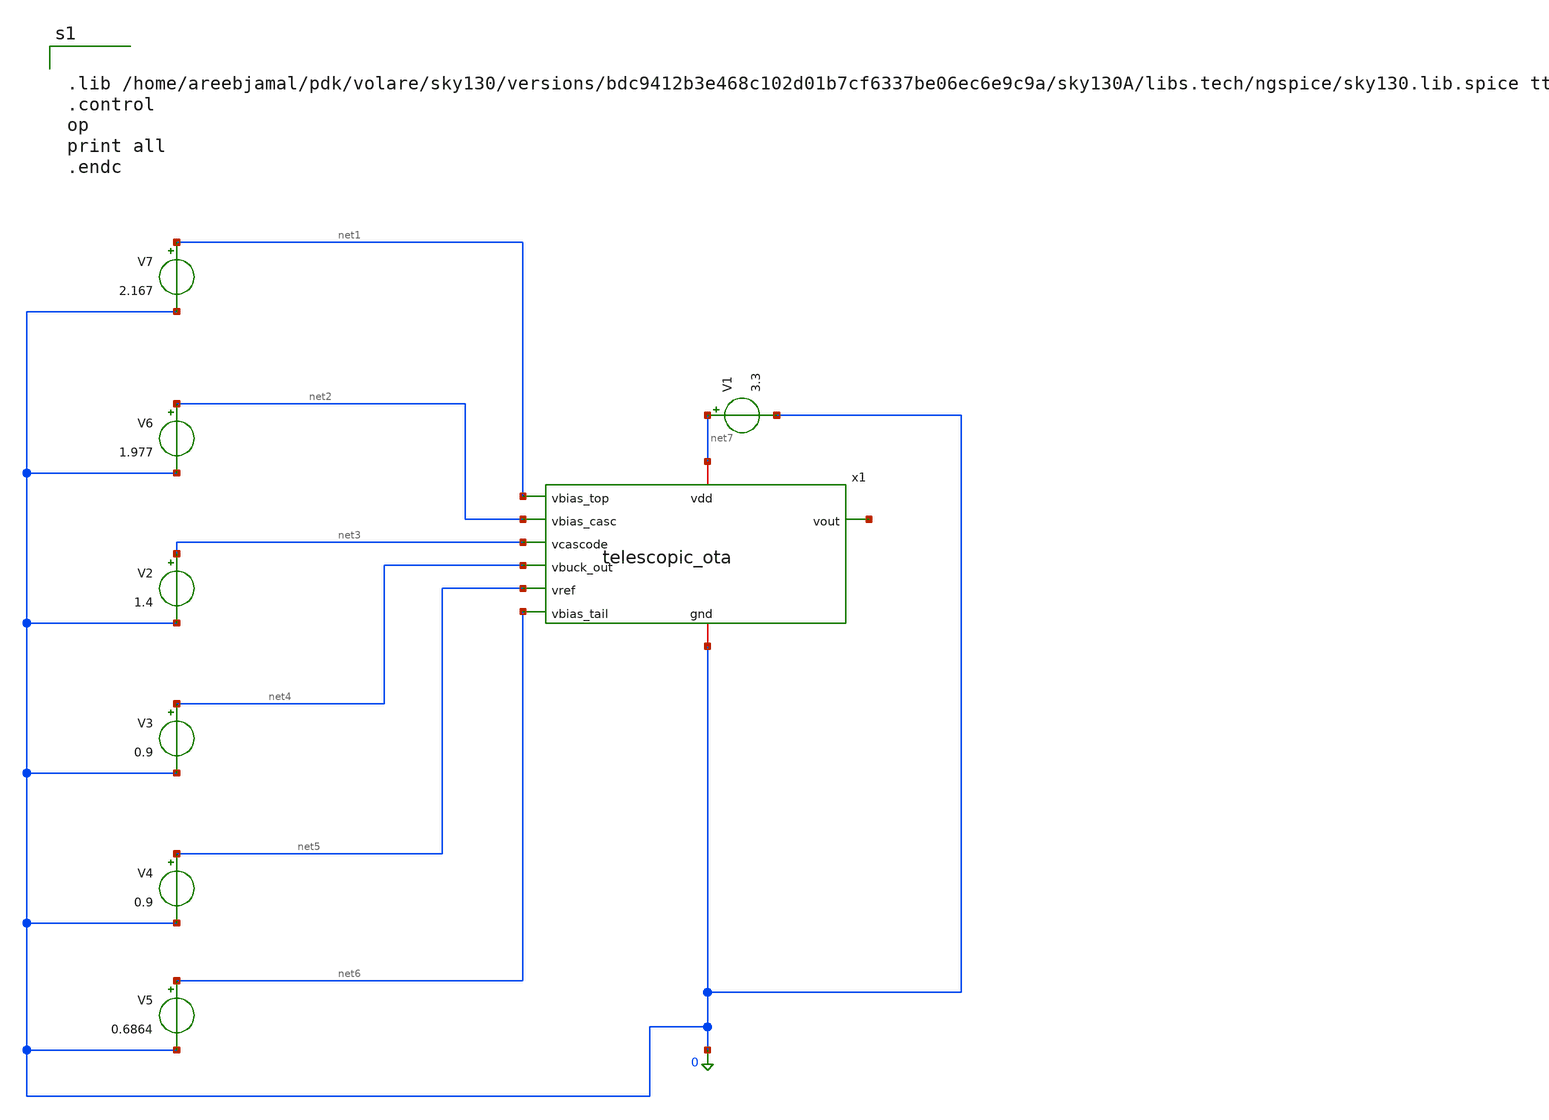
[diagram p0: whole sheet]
** sch_path: test_ota.sch
**.subckt test_ota
x1 net7 net1 net2 net8 net3 net4 net5 net6 0 telescopic_ota
V2 net3 0 1.4
V3 net4 0 0.9
V4 net5 0 0.9
V5 net6 0 0.6864
V6 net2 0 1.977
V7 net1 0 2.167
V1 net7 0 3.3
**** begin user architecture code


.lib /home/areebjamal/pdk/volare/sky130/versions/bdc9412b3e468c102d01b7cf6337be06ec6e9c9a/sky130A/libs.tech/ngspice/sky130.lib.spice tt
.control
op
print all
.endc


**** end user architecture code
**.ends

* expanding   symbol:  telescopic_ota.sym # of pins=9
** sym_path: telescopic_ota.sym
** sch_path: telescopic_ota.sch
.subckt telescopic_ota vdd vbias_top vbias_casc vout vcascode vbuck_out vref vbias_tail gnd
*.ipin vbias_top
*.ipin vbias_casc
*.ipin vcascode
*.ipin vbuck_out
*.ipin vref
*.ipin vbias_tail
*.opin vout
*.iopin vdd
*.iopin gnd
XM3 net3 vcascode vy gnd sky130_fd_pr__nfet_01v8 L=1 W=5.6 nf=1 ad='int((1 + 1)/2) * 5.6 / 1 * 0.29'
+ as='int((1 + 2)/2) * 5.6 / 1 * 0.29' pd='2*int((1 + 1)/2) * (5.6 / 1 + 0.29)' ps='2*int((1 + 2)/2) * (5.6 / 1 + 0.29)'
+ nrd='0.29 / 5.6 ' nrs='0.29 / 5.6 ' sa=0 sb=0 sd=0 mult=1 m=1
XM8 net2 vbias_top vdd vdd sky130_fd_pr__pfet_01v8 L=1 W=16.8 nf=1 ad='int((1 + 1)/2) * 16.8 / 1 * 0.29'
+ as='int((1 + 2)/2) * 16.8 / 1 * 0.29' pd='2*int((1 + 1)/2) * (16.8 / 1 + 0.29)' ps='2*int((1 + 2)/2) * (16.8 / 1 + 0.29)'
+ nrd='0.29 / 16.8 ' nrs='0.29 / 16.8 ' sa=0 sb=0 sd=0 mult=1 m=1
XM7 net1 vbias_top vdd vdd sky130_fd_pr__pfet_01v8 L=1 W=16.8 nf=1 ad='int((1 + 1)/2) * 16.8 / 1 * 0.29'
+ as='int((1 + 2)/2) * 16.8 / 1 * 0.29' pd='2*int((1 + 1)/2) * (16.8 / 1 + 0.29)' ps='2*int((1 + 2)/2) * (16.8 / 1 + 0.29)'
+ nrd='0.29 / 16.8 ' nrs='0.29 / 16.8 ' sa=0 sb=0 sd=0 mult=1 m=1
XM5 net3 vbias_casc net1 vdd sky130_fd_pr__pfet_01v8 L=1 W=16.8 nf=1 ad='int((1 + 1)/2) * 16.8 / 1 * 0.29'
+ as='int((1 + 2)/2) * 16.8 / 1 * 0.29' pd='2*int((1 + 1)/2) * (16.8 / 1 + 0.29)' ps='2*int((1 + 2)/2) * (16.8 / 1 + 0.29)'
+ nrd='0.29 / 16.8 ' nrs='0.29 / 16.8 ' sa=0 sb=0 sd=0 mult=1 m=1
XM6 vout vbias_casc net2 vdd sky130_fd_pr__pfet_01v8 L=1 W=16.8 nf=1 ad='int((1 + 1)/2) * 16.8 / 1 * 0.29'
+ as='int((1 + 2)/2) * 16.8 / 1 * 0.29' pd='2*int((1 + 1)/2) * (16.8 / 1 + 0.29)' ps='2*int((1 + 2)/2) * (16.8 / 1 + 0.29)'
+ nrd='0.29 / 16.8 ' nrs='0.29 / 16.8 ' sa=0 sb=0 sd=0 mult=1 m=1
XM1 vy vbuck_out net5 gnd sky130_fd_pr__nfet_01v8 L=1 W=5.6 nf=1 ad='int((1 + 1)/2) * 5.6 / 1 * 0.29'
+ as='int((1 + 2)/2) * 5.6 / 1 * 0.29' pd='2*int((1 + 1)/2) * (5.6 / 1 + 0.29)' ps='2*int((1 + 2)/2) * (5.6 / 1 + 0.29)'
+ nrd='0.29 / 5.6 ' nrs='0.29 / 5.6 ' sa=0 sb=0 sd=0 mult=1 m=1
XM4 vout vcascode net4 gnd sky130_fd_pr__nfet_01v8 L=1 W=5.6 nf=1 ad='int((1 + 1)/2) * 5.6 / 1 * 0.29'
+ as='int((1 + 2)/2) * 5.6 / 1 * 0.29' pd='2*int((1 + 1)/2) * (5.6 / 1 + 0.29)' ps='2*int((1 + 2)/2) * (5.6 / 1 + 0.29)'
+ nrd='0.29 / 5.6 ' nrs='0.29 / 5.6 ' sa=0 sb=0 sd=0 mult=1 m=1
XM2 net4 vref net5 gnd sky130_fd_pr__nfet_01v8 L=1 W=5.6 nf=1 ad='int((1 + 1)/2) * 5.6 / 1 * 0.29' as='int((1 + 2)/2) * 5.6 / 1 * 0.29'
+ pd='2*int((1 + 1)/2) * (5.6 / 1 + 0.29)' ps='2*int((1 + 2)/2) * (5.6 / 1 + 0.29)' nrd='0.29 / 5.6 ' nrs='0.29 / 5.6 '
+ sa=0 sb=0 sd=0 mult=1 m=1
XM9 net5 vbias_tail gnd gnd sky130_fd_pr__nfet_01v8 L=1 W=11.2 nf=1 ad='int((1 + 1)/2) * 11.2 / 1 * 0.29'
+ as='int((1 + 2)/2) * 11.2 / 1 * 0.29' pd='2*int((1 + 1)/2) * (11.2 / 1 + 0.29)' ps='2*int((1 + 2)/2) * (11.2 / 1 + 0.29)'
+ nrd='0.29 / 11.2 ' nrs='0.29 / 11.2 ' sa=0 sb=0 sd=0 mult=1 m=1
R1 vout vcomp 360k m=1
C1 vcomp gnd 100p m=1
.ends

.end
